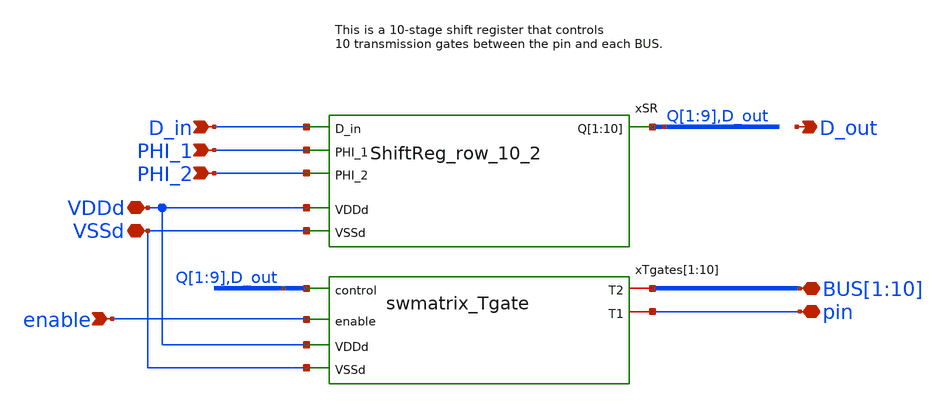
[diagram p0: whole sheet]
** sch_path: designs/switch_matrix/swmatrix_row_10/swmatrix_row_10.sch
**.subckt swmatrix_row_10 pin PHI_2 PHI_1
*+ BUS[1],BUS[2],BUS[3],BUS[4],BUS[5],BUS[6],BUS[7],BUS[8],BUS[9],BUS[10] D_in D_out VDDd VSSd enable
*.iopin pin
*.ipin PHI_2
*.ipin PHI_1
*.iopin BUS[1],BUS[2],BUS[3],BUS[4],BUS[5],BUS[6],BUS[7],BUS[8],BUS[9],BUS[10]
*.ipin D_in
*.opin D_out
*.iopin VDDd
*.iopin VSSd
*.ipin enable
xSR Q[1] Q[2] Q[3] Q[4] Q[5] Q[6] Q[7] Q[8] Q[9] D_out D_in PHI_1 PHI_2 VDDd VSSd ShiftReg_row_10_2
xTgates[1] Q[1] BUS[1] pin VDDd VSSd enable swmatrix_Tgate
xTgates[2] Q[2] BUS[2] pin VDDd VSSd enable swmatrix_Tgate
xTgates[3] Q[3] BUS[3] pin VDDd VSSd enable swmatrix_Tgate
xTgates[4] Q[4] BUS[4] pin VDDd VSSd enable swmatrix_Tgate
xTgates[5] Q[5] BUS[5] pin VDDd VSSd enable swmatrix_Tgate
xTgates[6] Q[6] BUS[6] pin VDDd VSSd enable swmatrix_Tgate
xTgates[7] Q[7] BUS[7] pin VDDd VSSd enable swmatrix_Tgate
xTgates[8] Q[8] BUS[8] pin VDDd VSSd enable swmatrix_Tgate
xTgates[9] Q[9] BUS[9] pin VDDd VSSd enable swmatrix_Tgate
xTgates[10] D_out BUS[10] pin VDDd VSSd enable swmatrix_Tgate
**.ends
.end
